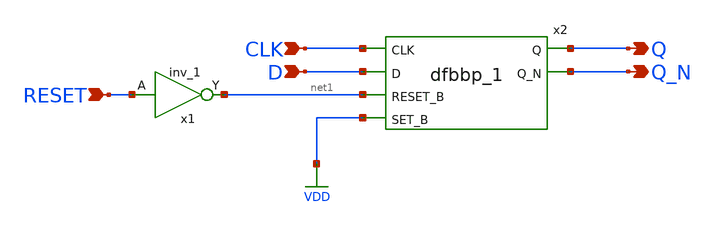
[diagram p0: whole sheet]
** sch_path: xschem/my_df2.sch
**.subckt my_df2 CLK D RESET Q Q_N
*.ipin CLK
*.ipin D
*.ipin RESET
*.opin Q
*.opin Q_N
x1 RESET GND GND VDD VDD net1 sky130_fd_sc_hd__inv_1
x2 CLK D net1 VDD GND GND VDD VDD Q Q_N sky130_fd_sc_hd__dfbbp_1
**.ends
.GLOBAL VDD
.end
